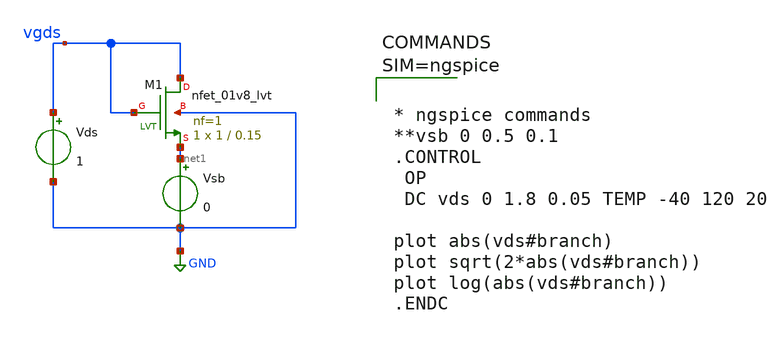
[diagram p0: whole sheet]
** sch_path: xschem/task.sch
**.subckt task
XM1 vgds vgds net1 GND sky130_fd_pr__nfet_01v8_lvt L=0.15 W=1 nf=1 ad='int((1 + 1)/2) * 1 / 1 * 0.29'
+ as='int((1 + 2)/2) * 1 / 1 * 0.29' pd='2*int((1 + 1)/2) * (1 / 1 + 0.29)' ps='2*int((1 + 2)/2) * (1 / 1 + 0.29)'
+ nrd='0.29 / 1 ' nrs='0.29 / 1 ' sa=0 sb=0 sd=0 mult=1 m=1
Vds vgds GND 1
Vsb net1 GND 0
**** begin user architecture code



* ngspice commands
**vsb 0 0.5 0.1
.CONTROL
 OP
 DC vds 0 1.8 0.05 TEMP -40 120 20

plot abs(vds#branch)
plot sqrt(2*abs(vds#branch))
plot log(abs(vds#branch))
.ENDC




** opencircuitdesign pdks install
.lib $::SKYWATER_MODELS/sky130.lib.spice tt

**** end user architecture code
**.ends
.GLOBAL GND
.end
